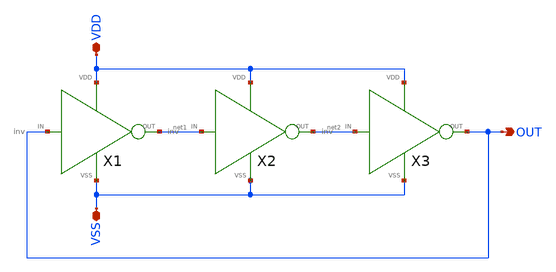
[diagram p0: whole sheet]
** sch_path: ringosc/ringosc.sch
**.subckt ringosc VDD VSS OUT
*.iopin VDD
*.iopin VSS
*.opin OUT
X1 OUT net1 VSS VDD inv
X2 net1 net2 VSS VDD inv
X3 net2 OUT VSS VDD inv
**** begin user architecture code

.include $::SKYWATER_MODELS/cells/nfet_01v8/sky130_fd_pr__nfet_01v8__tt.corner.spice
.include $::SKYWATER_MODELS/cells/nfet_01v8_lvt/sky130_fd_pr__nfet_01v8_lvt__tt.corner.spice
.include $::SKYWATER_MODELS/cells/pfet_01v8/sky130_fd_pr__pfet_01v8__tt.corner.spice
.include $::SKYWATER_MODELS/cells/nfet_03v3_nvt/sky130_fd_pr__nfet_03v3_nvt__tt.corner.spice
.include $::SKYWATER_MODELS/cells/nfet_05v0_nvt/sky130_fd_pr__nfet_05v0_nvt__tt.corner.spice
.include $::SKYWATER_MODELS/cells/esd_nfet_01v8/sky130_fd_pr__esd_nfet_01v8__tt.corner.spice
.include $::SKYWATER_MODELS/cells/pfet_01v8_lvt/sky130_fd_pr__pfet_01v8_lvt__tt.corner.spice
.include $::SKYWATER_MODELS/cells/pfet_01v8_hvt/sky130_fd_pr__pfet_01v8_hvt__tt.corner.spice
.include $::SKYWATER_MODELS/cells/esd_pfet_g5v0d10v5/sky130_fd_pr__esd_pfet_g5v0d10v5__tt.corner.spice
.include $::SKYWATER_MODELS/cells/pfet_g5v0d10v5/sky130_fd_pr__pfet_g5v0d10v5__tt.corner.spice
.include $::SKYWATER_MODELS/cells/pfet_g5v0d16v0/sky130_fd_pr__pfet_g5v0d16v0__tt.corner.spice
.include $::SKYWATER_MODELS/cells/nfet_g5v0d10v5/sky130_fd_pr__nfet_g5v0d10v5__tt.corner.spice
.include $::SKYWATER_MODELS/cells/nfet_g5v0d16v0/sky130_fd_pr__nfet_g5v0d16v0__tt_discrete.corner.spice
.include $::SKYWATER_MODELS/cells/esd_nfet_g5v0d10v5/sky130_fd_pr__esd_nfet_g5v0d10v5__tt.corner.spice
.include $::SKYWATER_MODELS/models/corners/tt/nonfet.spice
* Mismatch parameters
.include $::SKYWATER_MODELS/cells/nfet_01v8/sky130_fd_pr__nfet_01v8__mismatch.corner.spice
.include $::SKYWATER_MODELS/cells/pfet_01v8/sky130_fd_pr__pfet_01v8__mismatch.corner.spice
.include $::SKYWATER_MODELS/cells/nfet_01v8_lvt/sky130_fd_pr__nfet_01v8_lvt__mismatch.corner.spice
.include $::SKYWATER_MODELS/cells/pfet_01v8_lvt/sky130_fd_pr__pfet_01v8_lvt__mismatch.corner.spice
.include $::SKYWATER_MODELS/cells/pfet_01v8_hvt/sky130_fd_pr__pfet_01v8_hvt__mismatch.corner.spice
.include $::SKYWATER_MODELS/cells/nfet_g5v0d10v5/sky130_fd_pr__nfet_g5v0d10v5__mismatch.corner.spice
.include $::SKYWATER_MODELS/cells/pfet_g5v0d10v5/sky130_fd_pr__pfet_g5v0d10v5__mismatch.corner.spice
.include $::SKYWATER_MODELS/cells/nfet_05v0_nvt/sky130_fd_pr__nfet_05v0_nvt__mismatch.corner.spice
.include $::SKYWATER_MODELS/cells/nfet_03v3_nvt/sky130_fd_pr__nfet_03v3_nvt__mismatch.corner.spice
* Resistor$::SKYWATER_MODELS/Capacitor
.include $::SKYWATER_MODELS/models/r+c/res_typical__cap_typical.spice
.include $::SKYWATER_MODELS/models/r+c/res_typical__cap_typical__lin.spice
* Special cells
.include $::SKYWATER_MODELS/models/corners/tt/specialized_cells.spice
* All models
.include $::SKYWATER_MODELS/models/all.spice
* Corner
.include $::SKYWATER_MODELS/models/corners/tt/rf.spice

**** end user architecture code
**.ends

* expanding   symbol:  /home/brito/sky130_opensource_skel/opencryo/ringosc/inv.sym # of pins=4
** sym_path: ringosc/inv.sym
** sch_path: ringosc/inv.sch
.subckt inv IN OUT VSS VDD
*.ipin IN
*.iopin VSS
*.opin OUT
*.iopin VDD
XM1 OUT IN VSS VSS sky130_fd_pr__nfet_01v8 L=0.15 W=1 nf=1 ad='int((nf+1)/2) * W/nf * 0.29' as='int((nf+2)/2) * W/nf * 0.29'
+ pd='2*int((nf+1)/2) * (W/nf + 0.29)' ps='2*int((nf+2)/2) * (W/nf + 0.29)' nrd='0.29 / W' nrs='0.29 / W'
+ sa=0 sb=0 sd=0 mult=1 m=1
XM2 OUT IN VDD VDD sky130_fd_pr__pfet_01v8 L=0.15 W=1 nf=1 ad='int((nf+1)/2) * W/nf * 0.29' as='int((nf+2)/2) * W/nf * 0.29'
+ pd='2*int((nf+1)/2) * (W/nf + 0.29)' ps='2*int((nf+2)/2) * (W/nf + 0.29)' nrd='0.29 / W' nrs='0.29 / W'
+ sa=0 sb=0 sd=0 mult=1 m=1
.ends

**** begin user architecture code

* .option SCALE=1e-6
*.option method=gear seed=12
*.param L=0.15
*.param W=0.5

vdc vdd vss 1.8

.control
tran 1u 1n
.endc




**** end user architecture code
.end
